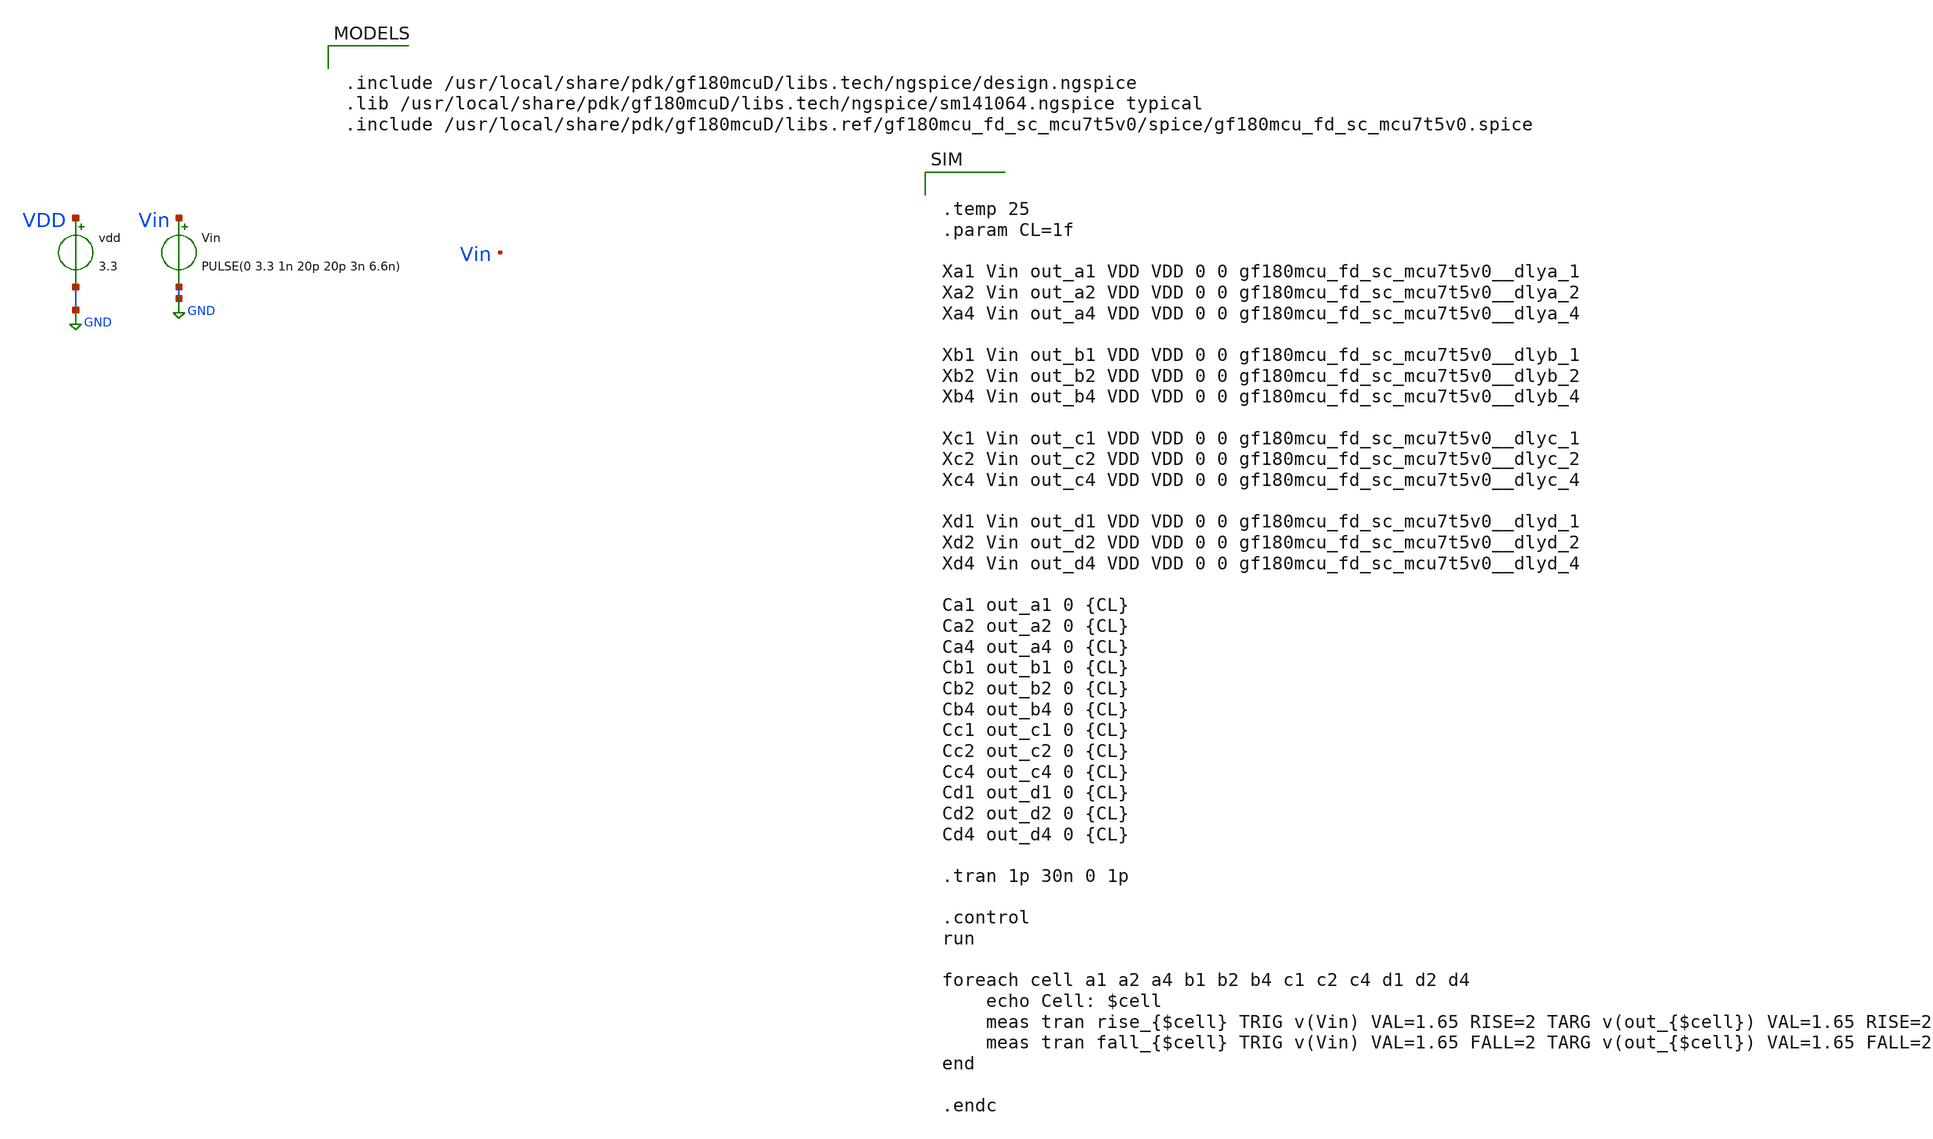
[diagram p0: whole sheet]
** sch_path: schem/pdk_delay_cell_test.sch
**.subckt pdk_delay_cell_test
Vin Vin GND PULSE(0 3.3 1n 20p 20p 3n 6.6n)
vdd VDD GND 3.3
**** begin user architecture code


.include /usr/local/share/pdk/gf180mcuD/libs.tech/ngspice/design.ngspice
.lib /usr/local/share/pdk/gf180mcuD/libs.tech/ngspice/sm141064.ngspice typical
.include /usr/local/share/pdk/gf180mcuD/libs.ref/gf180mcu_fd_sc_mcu7t5v0/spice/gf180mcu_fd_sc_mcu7t5v0.spice




.temp 25
.param CL=1f

Xa1 Vin out_a1 VDD VDD 0 0 gf180mcu_fd_sc_mcu7t5v0__dlya_1
Xa2 Vin out_a2 VDD VDD 0 0 gf180mcu_fd_sc_mcu7t5v0__dlya_2
Xa4 Vin out_a4 VDD VDD 0 0 gf180mcu_fd_sc_mcu7t5v0__dlya_4

Xb1 Vin out_b1 VDD VDD 0 0 gf180mcu_fd_sc_mcu7t5v0__dlyb_1
Xb2 Vin out_b2 VDD VDD 0 0 gf180mcu_fd_sc_mcu7t5v0__dlyb_2
Xb4 Vin out_b4 VDD VDD 0 0 gf180mcu_fd_sc_mcu7t5v0__dlyb_4

Xc1 Vin out_c1 VDD VDD 0 0 gf180mcu_fd_sc_mcu7t5v0__dlyc_1
Xc2 Vin out_c2 VDD VDD 0 0 gf180mcu_fd_sc_mcu7t5v0__dlyc_2
Xc4 Vin out_c4 VDD VDD 0 0 gf180mcu_fd_sc_mcu7t5v0__dlyc_4

Xd1 Vin out_d1 VDD VDD 0 0 gf180mcu_fd_sc_mcu7t5v0__dlyd_1
Xd2 Vin out_d2 VDD VDD 0 0 gf180mcu_fd_sc_mcu7t5v0__dlyd_2
Xd4 Vin out_d4 VDD VDD 0 0 gf180mcu_fd_sc_mcu7t5v0__dlyd_4

Ca1 out_a1 0 {CL}
Ca2 out_a2 0 {CL}
Ca4 out_a4 0 {CL}
Cb1 out_b1 0 {CL}
Cb2 out_b2 0 {CL}
Cb4 out_b4 0 {CL}
Cc1 out_c1 0 {CL}
Cc2 out_c2 0 {CL}
Cc4 out_c4 0 {CL}
Cd1 out_d1 0 {CL}
Cd2 out_d2 0 {CL}
Cd4 out_d4 0 {CL}

.tran 1p 30n 0 1p

.control
run

foreach cell a1 a2 a4 b1 b2 b4 c1 c2 c4 d1 d2 d4
    echo Cell: $cell
    meas tran rise_{$cell} TRIG v(Vin) VAL=1.65 RISE=2 TARG v(out_{$cell}) VAL=1.65 RISE=2
    meas tran fall_{$cell} TRIG v(Vin) VAL=1.65 FALL=2 TARG v(out_{$cell}) VAL=1.65 FALL=2
end

.endc


**** end user architecture code
**.ends
.GLOBAL GND
.end
